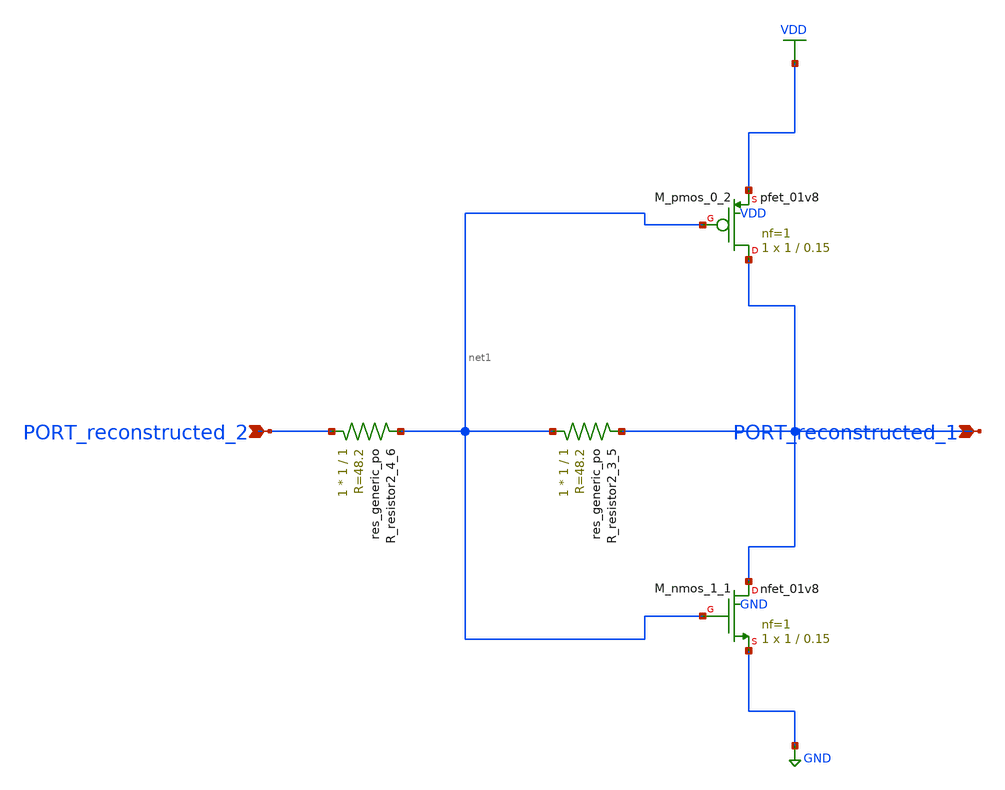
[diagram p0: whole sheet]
** sch_path: schematics/AMSNet/620.sch
**.subckt 620 PORT_reconstructed_1 PORT_reconstructed_2
*.ipin PORT_reconstructed_1
*.ipin PORT_reconstructed_2
XM_nmos_1_1 PORT_reconstructed_1 net1 GND GND sky130_fd_pr__nfet_01v8 L=0.15 W=1 nf=1 ad='int((1 + 1)/2) * 1 / 1 * 0.29'
+ as='int((1 + 2)/2) * 1 / 1 * 0.29' pd='2*int((1 + 1)/2) * (1 / 1 + 0.29)' ps='2*int((1 + 2)/2) * (1 / 1 + 0.29)'
+ nrd='0.29 / 1 ' nrs='0.29 / 1 ' sa=0 sb=0 sd=0 mult=1 m=1
XM_pmos_0_2 PORT_reconstructed_1 net1 VDD VDD sky130_fd_pr__pfet_01v8 L=0.15 W=1 nf=1 ad='int((1 + 1)/2) * 1 / 1 * 0.29'
+ as='int((1 + 2)/2) * 1 / 1 * 0.29' pd='2*int((1 + 1)/2) * (1 / 1 + 0.29)' ps='2*int((1 + 2)/2) * (1 / 1 + 0.29)'
+ nrd='0.29 / 1 ' nrs='0.29 / 1 ' sa=0 sb=0 sd=0 mult=1 m=1
XR_resistor2_3_5 net1 PORT_reconstructed_1 sky130_fd_pr__res_generic_po W=1 L=1 m=1
XR_resistor2_4_6 PORT_reconstructed_2 net1 sky130_fd_pr__res_generic_po W=1 L=1 m=1
**.ends
.GLOBAL GND
.GLOBAL VDD
.end
